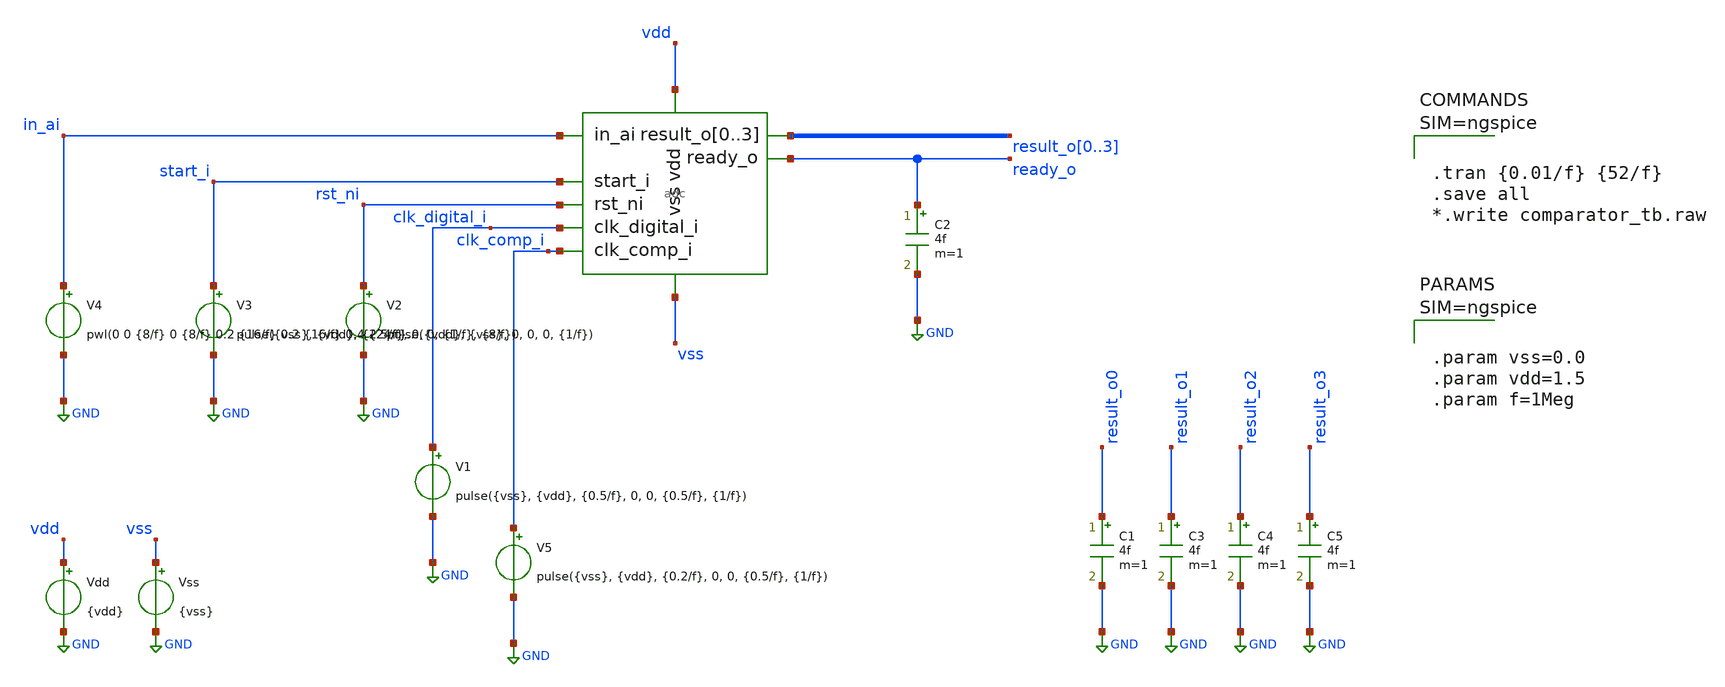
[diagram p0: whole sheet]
** sch_path: designs/basic1/adc_tb.sch
**.subckt adc_tb
x1 in_ai start_i rst_ni clk_digital_i result_o0 result_o1 result_o2 result_o3 ready_o vdd vss
+ clk_comp_i adc
V1 clk_digital_i GND pulse({vss}, {vdd}, {0.5/f}, 0, 0, {0.5/f}, {1/f})
V2 rst_ni GND pulse({vdd}, {vss}, 0, 0, 0, {1/f})
V3 start_i GND pulse({vss}, {vdd}, {2.5/f}, 0, 0, {1/f}, {8/f})
V4 in_ai GND pwl(0 0 {8/f} 0 {8/f} 0.2 {16/f} 0.2 {16/f} 0.4 {24/f} 0.4 {24/f} 0.6 {32/f} 0.6 {32/f}
+ 0.8 {40/f} 0.8 {40/f} 1.0 {52/f} 1.0)
.save i(v4)
Vdd vdd GND {vdd}
Vss vss GND {vss}
C1 result_o0 GND 4f m=1
C2 ready_o GND 4f m=1
C3 result_o1 GND 4f m=1
C4 result_o2 GND 4f m=1
C5 result_o3 GND 4f m=1
V5 clk_comp_i GND pulse({vss}, {vdd}, {0.2/f}, 0, 0, {0.5/f}, {1/f})
**** begin user architecture code

.lib $::SG13G2_MODELS/cornerMOSlv.lib mos_tt
.lib $::SG13G2_MODELS/cornerCAP.lib cap_typ
.include $::PDK_ROOT/ihp-sg13g2/libs.ref/sg13g2_stdcell/spice/sg13g2_stdcell.spice




.tran {0.01/f} {52/f}
.save all
*.write comparator_tb.raw






.param vss=0.0
.param vdd=1.5
.param f=1Meg






.model adc_buff_clk adc_bridge(in_low = 'vdd/2' in_high = 'vdd/2')

.control
pre_set auto_bridge_d_out =  ( ".model auto_bridge_out bidi_bridge(direction=0 out_high=1.5
+ t_rise=1n t_fall=1n)"    "auto_bridge_out%d [ %s ] [ %s ] null auto_bridge_out" )
pre_set auto_bridge_d_in =  ( ".model auto_bridge_in bidi_bridge(direction=1 in_low=0.5 in_high=1)"
+    "auto_bridge_in%d [ %s ] [ %s ] null auto_bridge_in" )
.endc



**** end user architecture code
**.ends
.GLOBAL GND
.end
